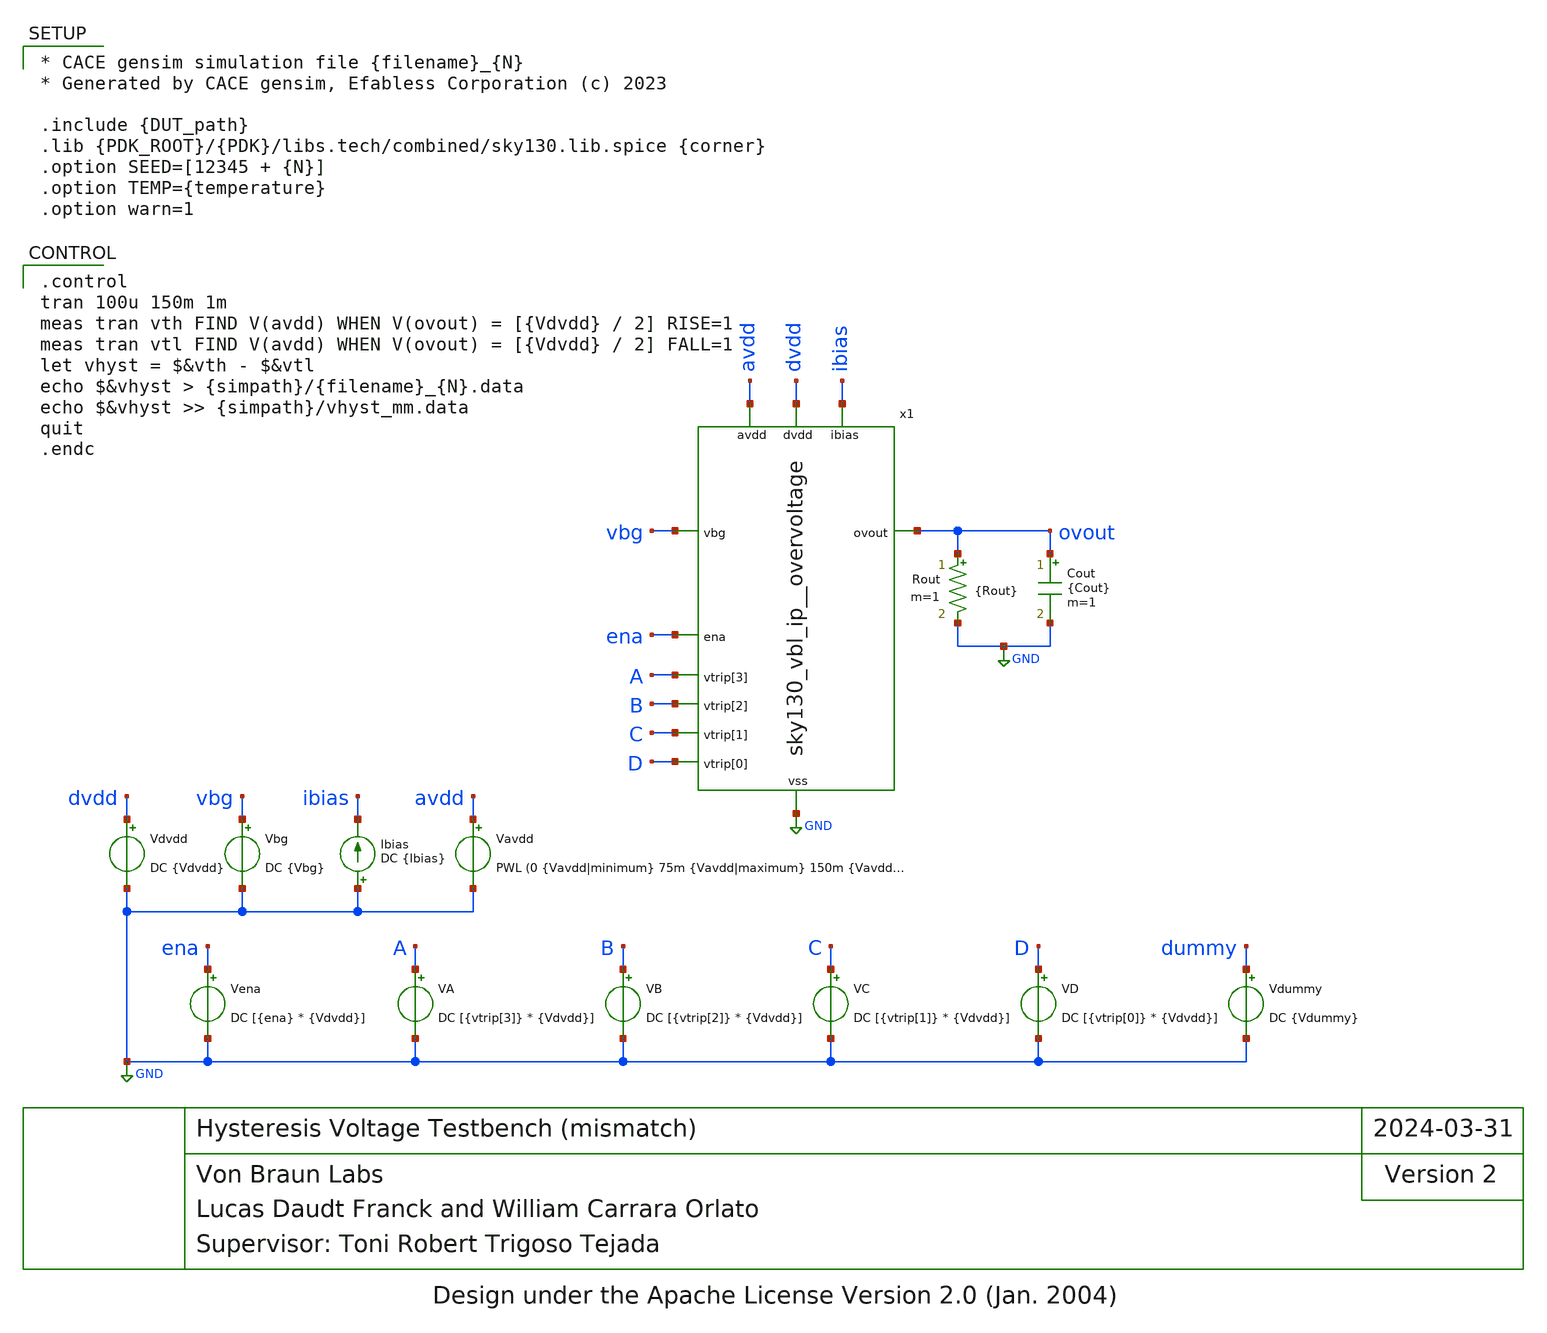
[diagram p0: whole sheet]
** sch_path: cace/tb_vhyst_mm.sch
* Design under the Apache License Version 2.0 (Jan. 2004)
**.subckt tb_vhyst_mm
Vavdd avdd GND PWL (0 {Vavdd|minimum} 75m {Vavdd|maximum} 150m {Vavdd|minimum})
Vdvdd dvdd GND DC {Vdvdd}
Vbg vbg GND DC {Vbg}
Ibias GND ibias DC {Ibias}
Vena ena GND DC [{ena} * {Vdvdd}]
VA A GND DC [{vtrip[3]} * {Vdvdd}]
VB B GND DC [{vtrip[2]} * {Vdvdd}]
VC C GND DC [{vtrip[1]} * {Vdvdd}]
VD D GND DC [{vtrip[0]} * {Vdvdd}]
Vdummy dummy GND DC {Vdummy}
Cout ovout GND {Cout} m=1
Rout ovout GND {Rout} m=1
x1 avdd dvdd ena A GND ibias B ovout vbg C D sky130_vbl_ip__overvoltage
**** begin user architecture code

* CACE gensim simulation file {filename}_{N}
* Generated by CACE gensim, Efabless Corporation (c) 2023

.include {DUT_path}
.lib {PDK_ROOT}/{PDK}/libs.tech/combined/sky130.lib.spice {corner}
.option SEED=[12345 + {N}]
.option TEMP={temperature}
.option warn=1


.control
tran 100u 150m 1m
meas tran vth FIND V(avdd) WHEN V(ovout) = [{Vdvdd} / 2] RISE=1
meas tran vtl FIND V(avdd) WHEN V(ovout) = [{Vdvdd} / 2] FALL=1
let vhyst = $&vth - $&vtl
echo $&vhyst > {simpath}/{filename}_{N}.data
echo $&vhyst >> {simpath}/vhyst_mm.data
quit
.endc


**** end user architecture code
**.ends
.GLOBAL GND
.end
